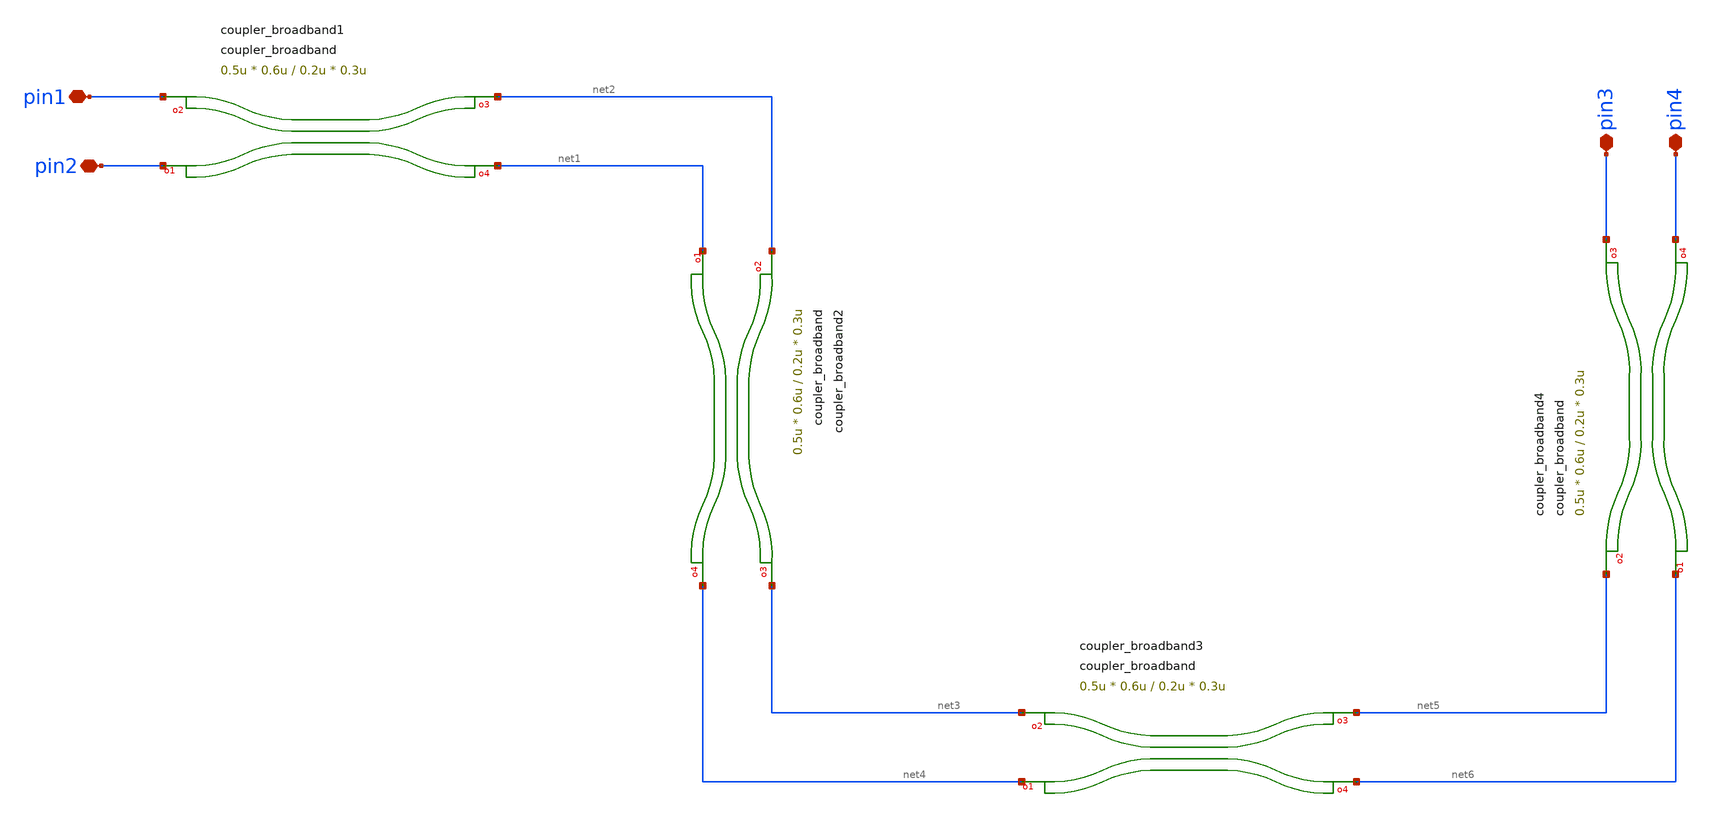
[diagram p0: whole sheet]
** sch_path: xschem/tests/test_sch/test_coupler_broadband.sch
* Copyright (c) 2024, Mabrains LLC
* Licensed under the GNU Lesser General Public License, Version 3.0 (the "License");
* you may not use this file except in compliance with the License.
* GNU Lesser General Public License
* Version 3, 29 June 2007
* This program is free software: you can redistribute it and/or modify
* it under the terms of the GNU Lesser General Public License as published
* by the Free Software Foundation, either version 3 of the License, or
* (at your option) any later version.
* This program is distributed in the hope that it will be useful,
* but WITHOUT ANY WARRANTY; without even the implied warranty of
* MERCHANTABILITY or FITNESS FOR A PARTICULAR PURPOSE.  See the
* GNU Lesser General Public License for more details.
* You should have received a copy of the GNU Lesser General Public License
* along with this program.  If not, see <https://www.gnu.org/licenses/>.
* SPDX-License-Identifier: LGPL-3.0
**.subckt test_coupler_broadband pin1 pin2 pin3 pin4
*.iopin pin1
*.iopin pin2
*.iopin pin3
*.iopin pin4
Pcoupler_broadband1 pin1 pin2 net2 net1 coupler_broadband w_sc=0.5u gap_sc=0.2u w_top=0.6u
+ gap_pc=0.3u length_taper=1.0u length_coupler_straight=12.4u length_coupler_big_gap=4.7u radius=10.0u
Pcoupler_broadband3 net3 net4 net5 net6 coupler_broadband w_sc=0.5u gap_sc=0.2u w_top=0.6u
+ gap_pc=0.3u length_taper=1.0u length_coupler_straight=12.4u length_coupler_big_gap=4.7u radius=10.0u
Pcoupler_broadband4 net5 net6 pin3 pin4 coupler_broadband w_sc=0.5u gap_sc=0.2u w_top=0.6u
+ gap_pc=0.3u length_taper=1.0u length_coupler_straight=12.4u length_coupler_big_gap=4.7u radius=10.0u
Pcoupler_broadband2 net2 net1 net3 net4 coupler_broadband w_sc=0.5u gap_sc=0.2u w_top=0.6u
+ gap_pc=0.3u length_taper=1.0u length_coupler_straight=12.4u length_coupler_big_gap=4.7u radius=10.0u
**.ends
.end
